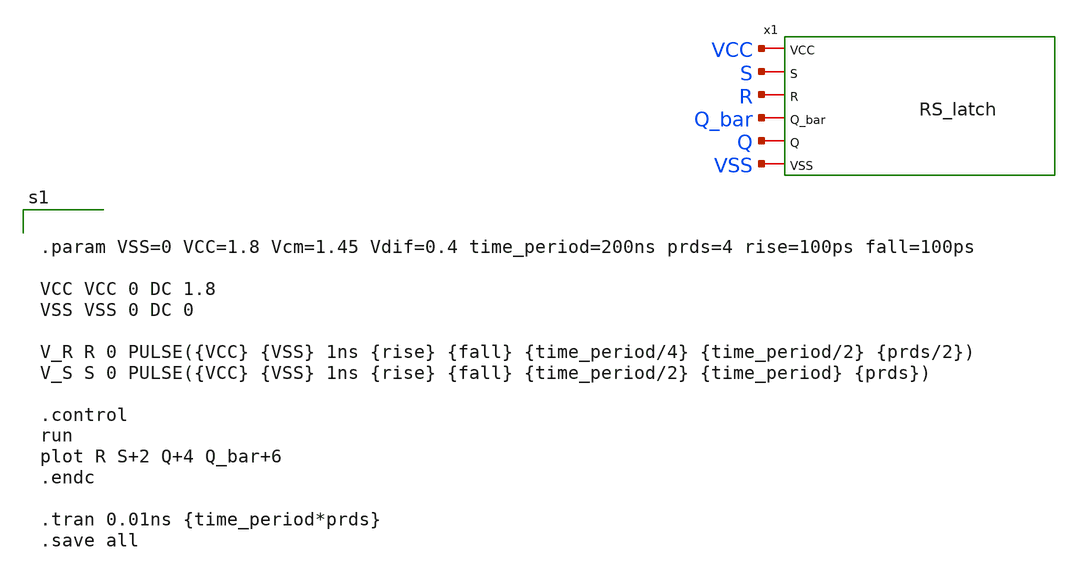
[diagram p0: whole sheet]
** sch_path: RS_latch/RS_latch_test.sch
**.subckt RS_latch_test
x1 VCC R S Q_bar Q VSS RS_latch
**** begin user architecture code


.param VSS=0 VCC=1.8 Vcm=1.45 Vdif=0.4 time_period=200ns prds=4 rise=100ps fall=100ps

VCC VCC 0 DC 1.8
VSS VSS 0 DC 0

V_R R 0 PULSE({VCC} {VSS} 1ns {rise} {fall} {time_period/4} {time_period/2} {prds/2})
V_S S 0 PULSE({VCC} {VSS} 1ns {rise} {fall} {time_period/2} {time_period} {prds})

.control
run
plot R S+2 Q+4 Q_bar+6
.endc

.tran 0.01ns {time_period*prds}
.save all



** opencircuitdesign pdks install
.lib $::SKYWATER_MODELS/sky130.lib.spice tt

**** end user architecture code
**.ends
.end
